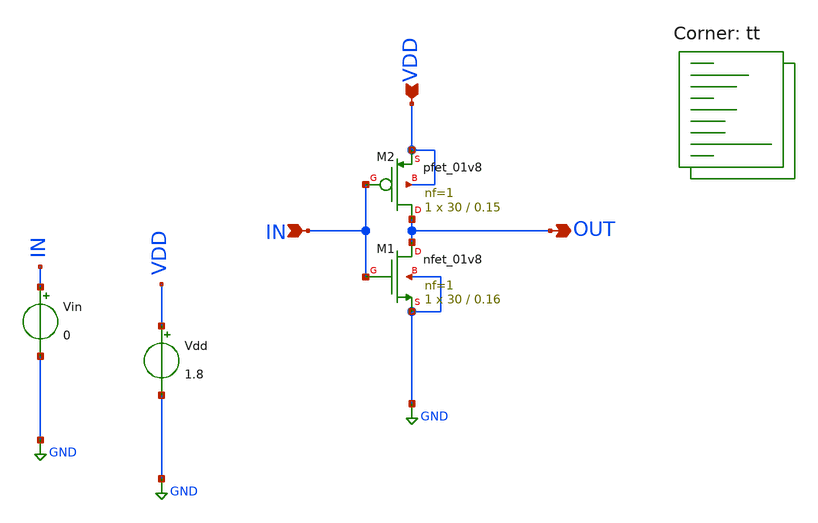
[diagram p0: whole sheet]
** sch_path: inverter.sch
**.subckt inverter IN VDD OUT
*.ipin IN
*.ipin VDD
*.opin OUT
Vin IN GND 0
Vdd VDD GND 1.8
XM1 OUT IN GND GND sky130_fd_pr__nfet_01v8 L=0.16 W=30 nf=1 ad='int((nf+1)/2) * W/nf * 0.29' as='int((nf+2)/2) * W/nf * 0.29'
+ pd='2*int((nf+1)/2) * (W/nf + 0.29)' ps='2*int((nf+2)/2) * (W/nf + 0.29)' nrd='0.29 / W' nrs='0.29 / W'
+ sa=0 sb=0 sd=0 mult=1 m=1
XM2 OUT IN VDD VDD sky130_fd_pr__pfet_01v8 L=0.15 W=30 nf=1 ad='int((nf+1)/2) * W/nf * 0.29' as='int((nf+2)/2) * W/nf * 0.29'
+ pd='2*int((nf+1)/2) * (W/nf + 0.29)' ps='2*int((nf+2)/2) * (W/nf + 0.29)' nrd='0.29 / W' nrs='0.29 / W'
+ sa=0 sb=0 sd=0 mult=1 m=1
**** begin user architecture code



.options savecurrents

.control
save all
dc vin 0 1.8 0.01
let id_nmos=@m.xm1.msky130_fd_pr__nfet_01v8[id]
let id_pmos=@m.xm2.msky130_fd_pr__pfet_01v8[id]

plot deriv(sqrt(id_nmos))^2/deriv(sqrt(id_pmos))^2

.endc


.lib $::SKYWATER_MODELS/sky130.lib.spice tt
**** end user architecture code
**.ends
.GLOBAL GND
.end
